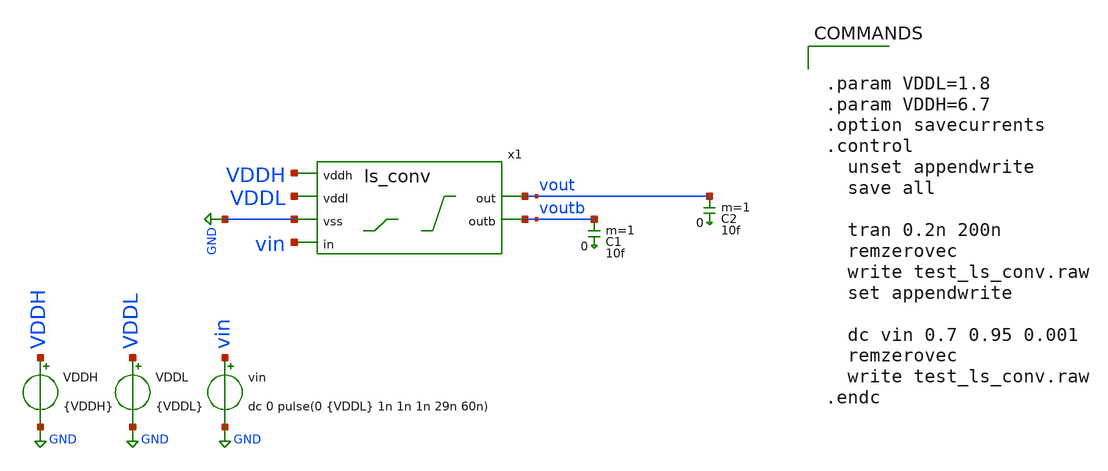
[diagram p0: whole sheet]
** sch_path: level_shifters/test_ls_conv.sch
**.subckt test_ls_conv
x1 vin vout voutb VDDL GND VDDH ls_conv
VDDL VDDL GND {VDDL}
VDDH VDDH GND {VDDH}
vin vin GND dc 0 pulse(0 {VDDL} 1n 1n 1n 29n 60n)
C1 voutb 0 10f m=1
C2 vout 0 10f m=1
**** begin user architecture code

** opencircuitdesign pdks install
.lib $::SKYWATER_MODELS/sky130.lib.spice tt



.param VDDL=1.8
.param VDDH=6.7
.option savecurrents
.control
  unset appendwrite
  save all

  tran 0.2n 200n
  remzerovec
  write test_ls_conv.raw
  set appendwrite

  dc vin 0.7 0.95 0.001
  remzerovec
  write test_ls_conv.raw
.endc


**** end user architecture code
**.ends

* expanding   symbol:  ls_conv.sym # of pins=6
** sym_path: level_shifters/ls_conv.sym
** sch_path: level_shifters/ls_conv.sch
.subckt ls_conv in out outb vddl vss vddh
*.ipin vddh
*.ipin vss
*.ipin vddl
*.ipin in
*.opin out
*.opin outb
XMN1 outb inb vss vss sky130_fd_pr__nfet_g5v0d10v5 L=0.5 W=5 nf=1 ad='int((nf+1)/2) * W/nf * 0.29' as='int((nf+2)/2) * W/nf * 0.29'
+ pd='2*int((nf+1)/2) * (W/nf + 0.29)' ps='2*int((nf+2)/2) * (W/nf + 0.29)' nrd='0.29 / W' nrs='0.29 / W'
+ sa=0 sb=0 sd=0 mult=1 m=1
XMN2 out inbb vss vss sky130_fd_pr__nfet_g5v0d10v5 L=0.5 W=5 nf=1 ad='int((nf+1)/2) * W/nf * 0.29' as='int((nf+2)/2) * W/nf * 0.29'
+ pd='2*int((nf+1)/2) * (W/nf + 0.29)' ps='2*int((nf+2)/2) * (W/nf + 0.29)' nrd='0.29 / W' nrs='0.29 / W'
+ sa=0 sb=0 sd=0 mult=1 m=1
XMP1 outb out vddh vddh sky130_fd_pr__pfet_g5v0d10v5 L=0.5 W=1 nf=1 ad='int((nf+1)/2) * W/nf * 0.29'
+ as='int((nf+2)/2) * W/nf * 0.29' pd='2*int((nf+1)/2) * (W/nf + 0.29)' ps='2*int((nf+2)/2) * (W/nf + 0.29)'
+ nrd='0.29 / W' nrs='0.29 / W' sa=0 sb=0 sd=0 mult=1 m=1
XMP2 out outb vddh vddh sky130_fd_pr__pfet_g5v0d10v5 L=0.5 W=1 nf=1 ad='int((nf+1)/2) * W/nf * 0.29'
+ as='int((nf+2)/2) * W/nf * 0.29' pd='2*int((nf+1)/2) * (W/nf + 0.29)' ps='2*int((nf+2)/2) * (W/nf + 0.29)'
+ nrd='0.29 / W' nrs='0.29 / W' sa=0 sb=0 sd=0 mult=1 m=1
XM1 inb in vss vss sky130_fd_pr__nfet_01v8 L=0.15 W=1 nf=1 ad='int((nf+1)/2) * W/nf * 0.29' as='int((nf+2)/2) * W/nf * 0.29'
+ pd='2*int((nf+1)/2) * (W/nf + 0.29)' ps='2*int((nf+2)/2) * (W/nf + 0.29)' nrd='0.29 / W' nrs='0.29 / W'
+ sa=0 sb=0 sd=0 mult=1 m=1
XM2 inb in vddl vddl sky130_fd_pr__pfet_01v8 L=0.15 W=1 nf=1 ad='int((nf+1)/2) * W/nf * 0.29' as='int((nf+2)/2) * W/nf * 0.29'
+ pd='2*int((nf+1)/2) * (W/nf + 0.29)' ps='2*int((nf+2)/2) * (W/nf + 0.29)' nrd='0.29 / W' nrs='0.29 / W'
+ sa=0 sb=0 sd=0 mult=1 m=1
XM3 inbb inb vss vss sky130_fd_pr__nfet_01v8 L=0.15 W=1 nf=1 ad='int((nf+1)/2) * W/nf * 0.29' as='int((nf+2)/2) * W/nf * 0.29'
+ pd='2*int((nf+1)/2) * (W/nf + 0.29)' ps='2*int((nf+2)/2) * (W/nf + 0.29)' nrd='0.29 / W' nrs='0.29 / W'
+ sa=0 sb=0 sd=0 mult=1 m=1
XM4 inbb inb vddl vddl sky130_fd_pr__pfet_01v8 L=0.15 W=1 nf=1 ad='int((nf+1)/2) * W/nf * 0.29' as='int((nf+2)/2) * W/nf * 0.29'
+ pd='2*int((nf+1)/2) * (W/nf + 0.29)' ps='2*int((nf+2)/2) * (W/nf + 0.29)' nrd='0.29 / W' nrs='0.29 / W'
+ sa=0 sb=0 sd=0 mult=1 m=1
.ends

.GLOBAL GND
.end
